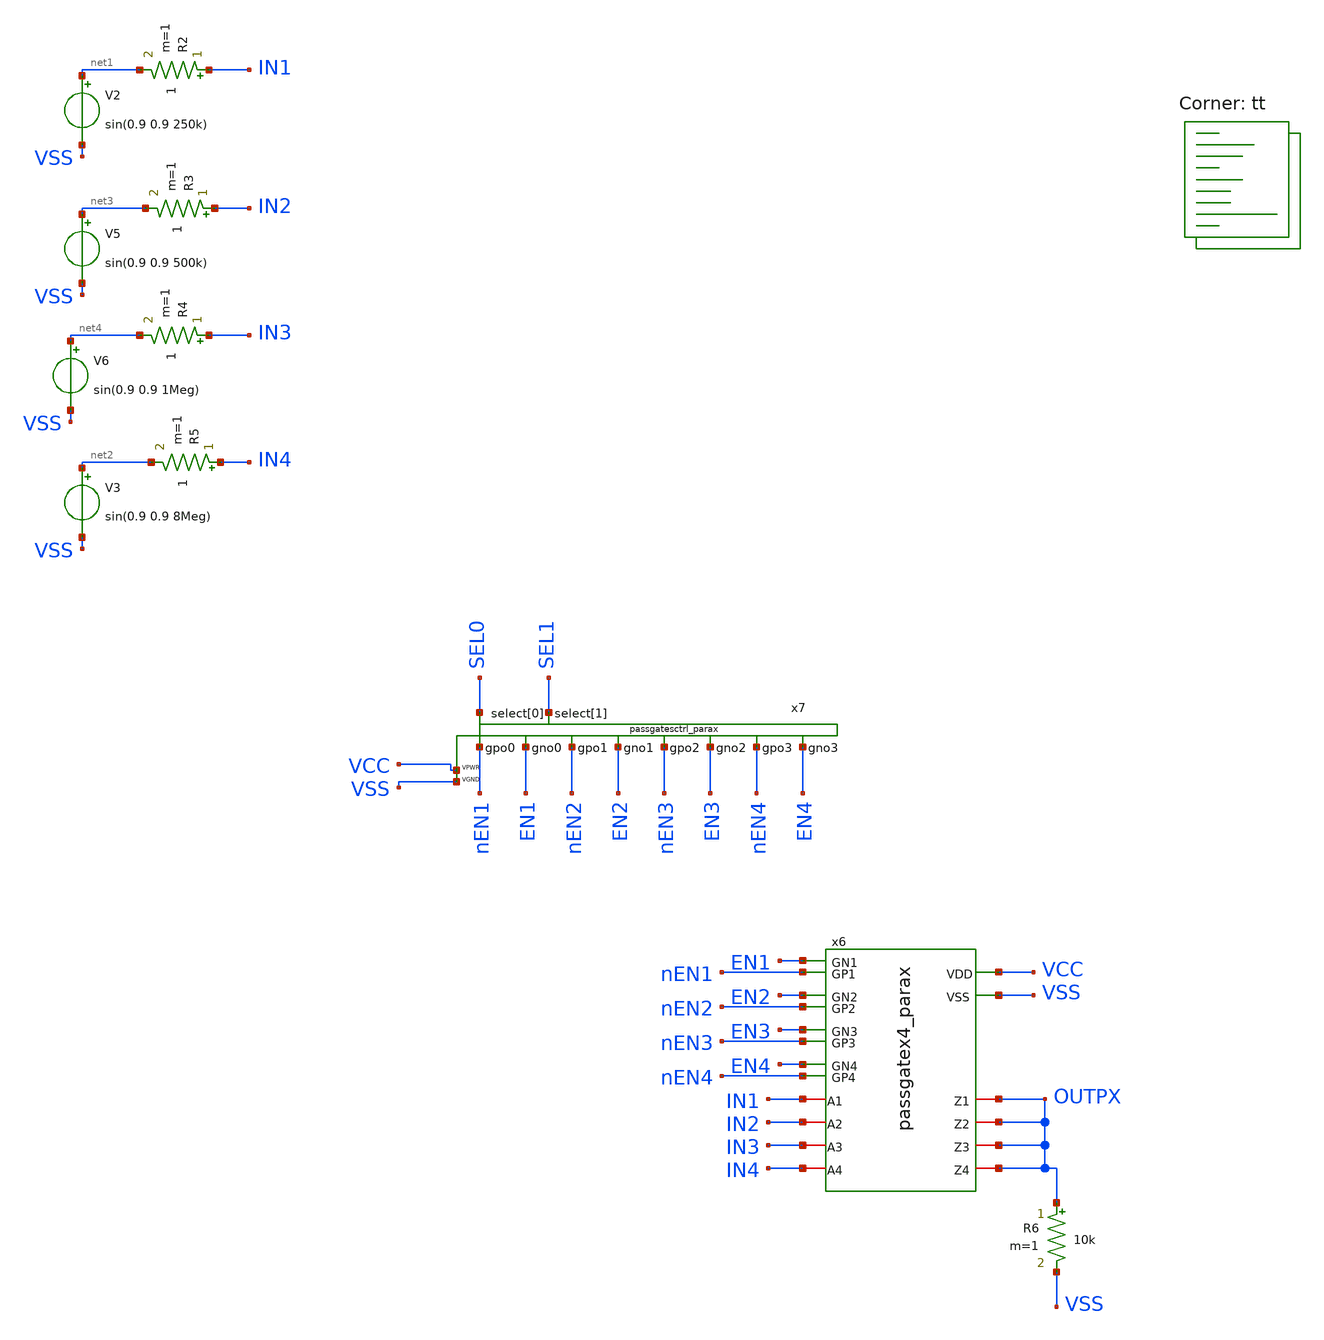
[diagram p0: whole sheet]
** sch_path: xschem/tb_4to1mux.sch
**.subckt tb_4to1mux
V2 net1 VSS sin(0.9 0.9 250k)
V3 net2 VSS sin(0.9 0.9 8Meg)
V5 net3 VSS sin(0.9 0.9 500k)
V6 net4 VSS sin(0.9 0.9 1Meg)
R2 IN1 net1 1 m=1
R3 IN2 net3 1 m=1
R4 IN3 net4 1 m=1
R5 IN4 net2 1 m=1
x6 nEN3 nEN2 nEN1 VCC nEN4 VSS IN3 IN2 IN1 OUTPX OUTPX OUTPX IN4 OUTPX EN3 EN2 EN1 EN4
+ passgatex4_parax
R6 OUTPX VSS 10k m=1
x7 VSS VCC EN1 EN2 EN3 EN4 nEN1 nEN2 nEN3 nEN4 SEL0 SEL1 passgatesctrl_parax
**** begin user architecture code
.lib $::SKYWATER_MODELS/sky130.lib.spice tt
**** end user architecture code
**.ends

* expanding   symbol:  /home/ttuser/work/tt09-analogmux/xschem/passgatex4_parax.sym # of pins=18
** sym_path: xschem/passgatex4.sym
.include [file normalize extracted/passgatex4_parax.spice]
**** begin user architecture code


* ngspice commands
* .options savecurrents
.param VCC = 1.8
.param SRCRES = 1k
.include stimuli_tb_4to1mux.cir
.control
save all
op
write tb_4to1muxraw
set appendwrite
tran 10n 33u
write tb_4to1mux.raw
quit 0
.endc



**** end user architecture code
.end
